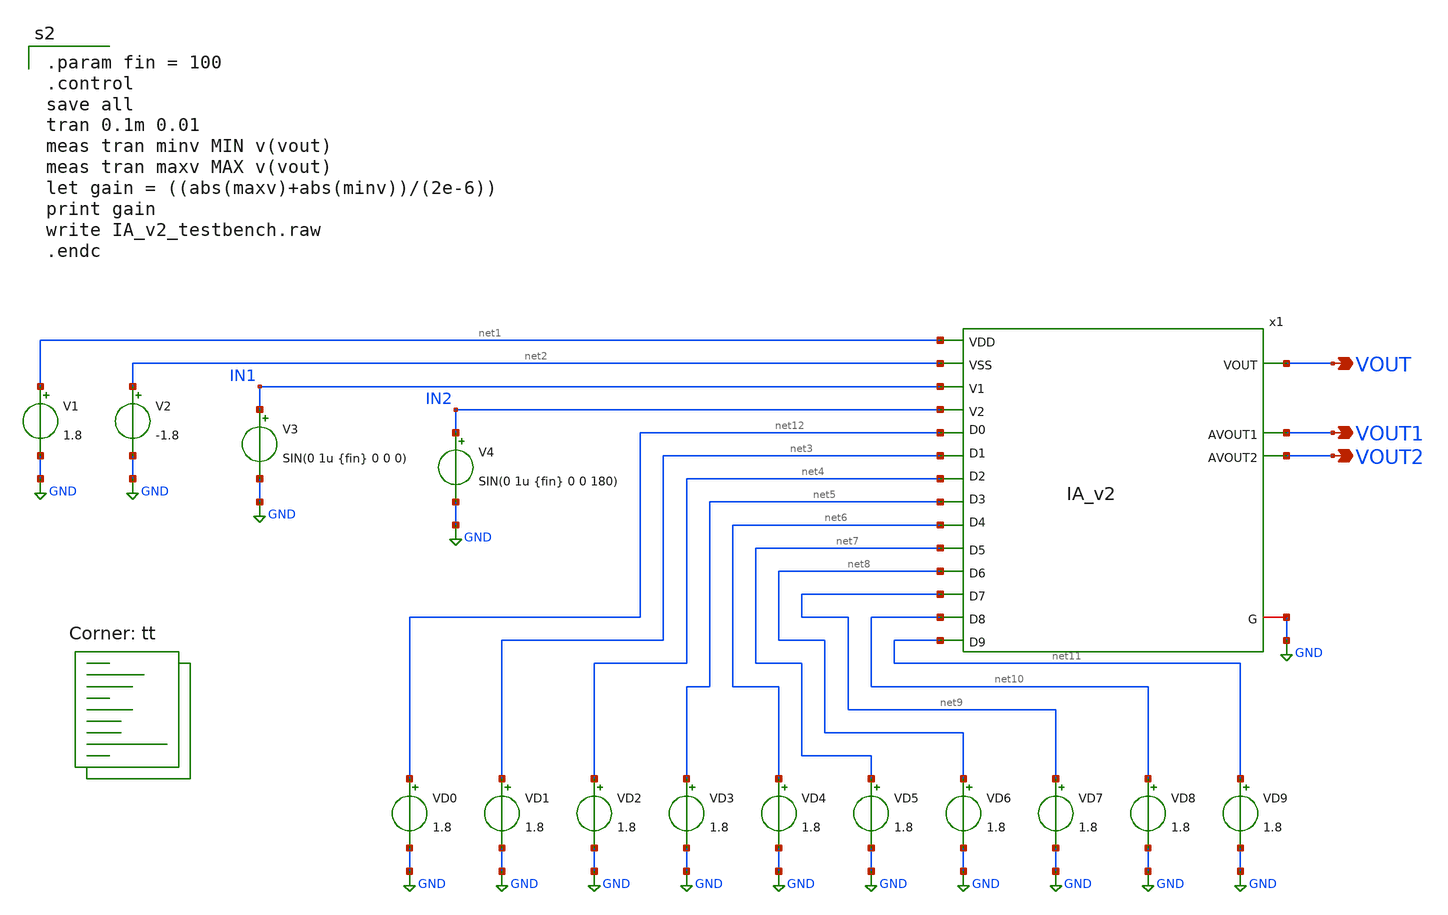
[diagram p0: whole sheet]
** sch_path: IA_v2_testbench.sch
**.subckt IA_v2_testbench VOUT VOUT1 VOUT2
*.opin VOUT
*.opin VOUT1
*.opin VOUT2
V1 net1 GND 1.8
V2 net2 GND -1.8
V3 IN1 GND SIN(0 1u {fin} 0 0 0)
V4 IN2 GND SIN(0 1u {fin} 0 0 180)
VD0 net12 GND 1.8
VD1 net3 GND 1.8
VD2 net4 GND 1.8
VD3 net5 GND 1.8
VD4 net6 GND 1.8
VD5 net7 GND 1.8
VD6 net8 GND 1.8
VD7 net9 GND 1.8
VD8 net10 GND 1.8
VD9 net11 GND 1.8
x1 VOUT1 net1 net2 VOUT IN1 IN2 VOUT2 net6 net5 net4 net3 net12 GND net8 net9 net10 net7 net11 IA_v2
**** begin user architecture code

.param fin = 100
.control
save all
tran 0.1m 0.01
meas tran minv MIN v(vout)
meas tran maxv MAX v(vout)
let gain = ((abs(maxv)+abs(minv))/(2e-6))
print gain
write IA_v2_testbench.raw
.endc

.lib $::SKYWATER_MODELS/sky130.lib.spice tt
**** end user architecture code
**.ends
.GLOBAL GND
.end
